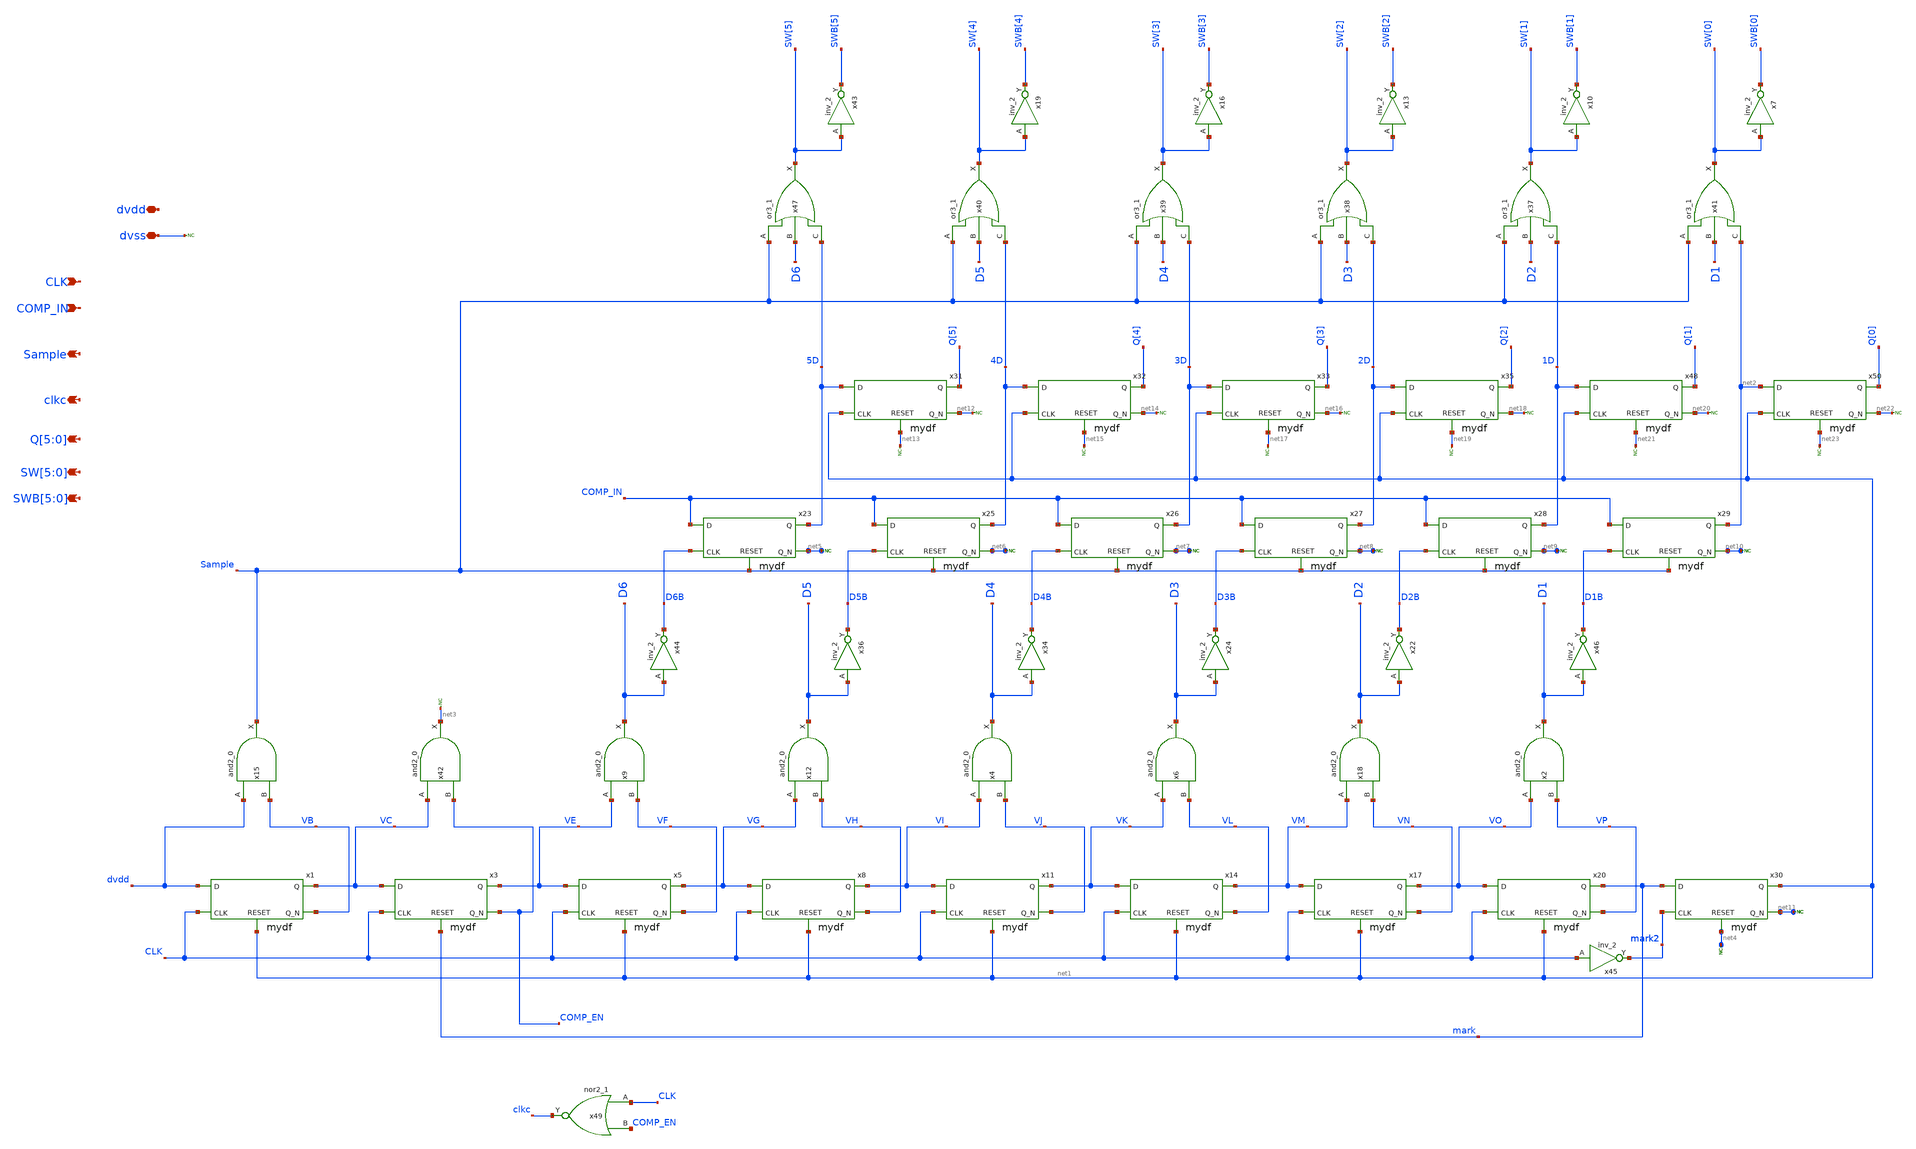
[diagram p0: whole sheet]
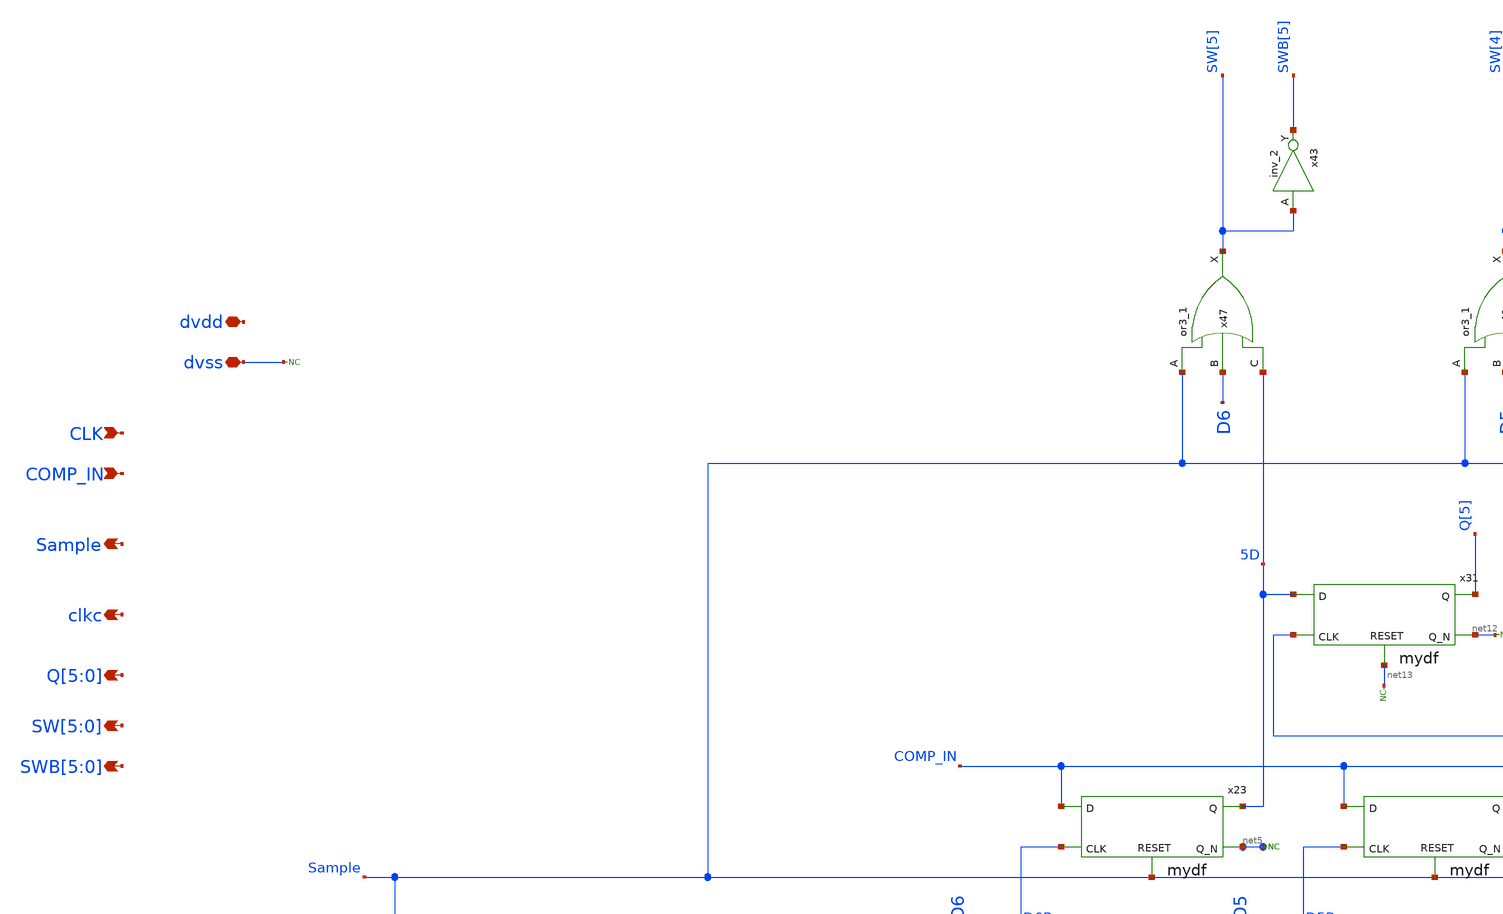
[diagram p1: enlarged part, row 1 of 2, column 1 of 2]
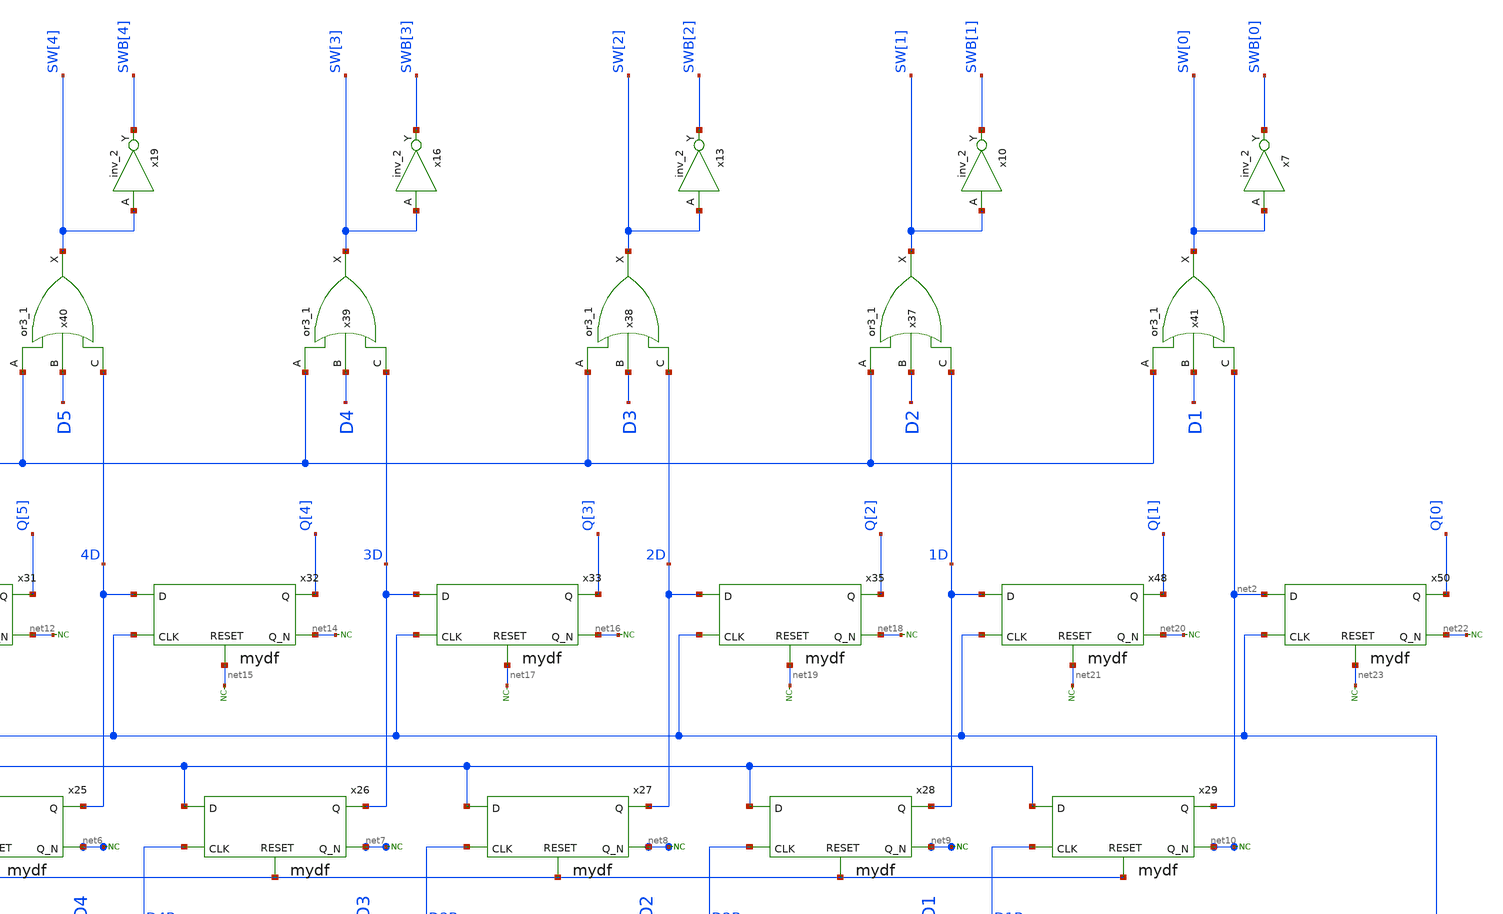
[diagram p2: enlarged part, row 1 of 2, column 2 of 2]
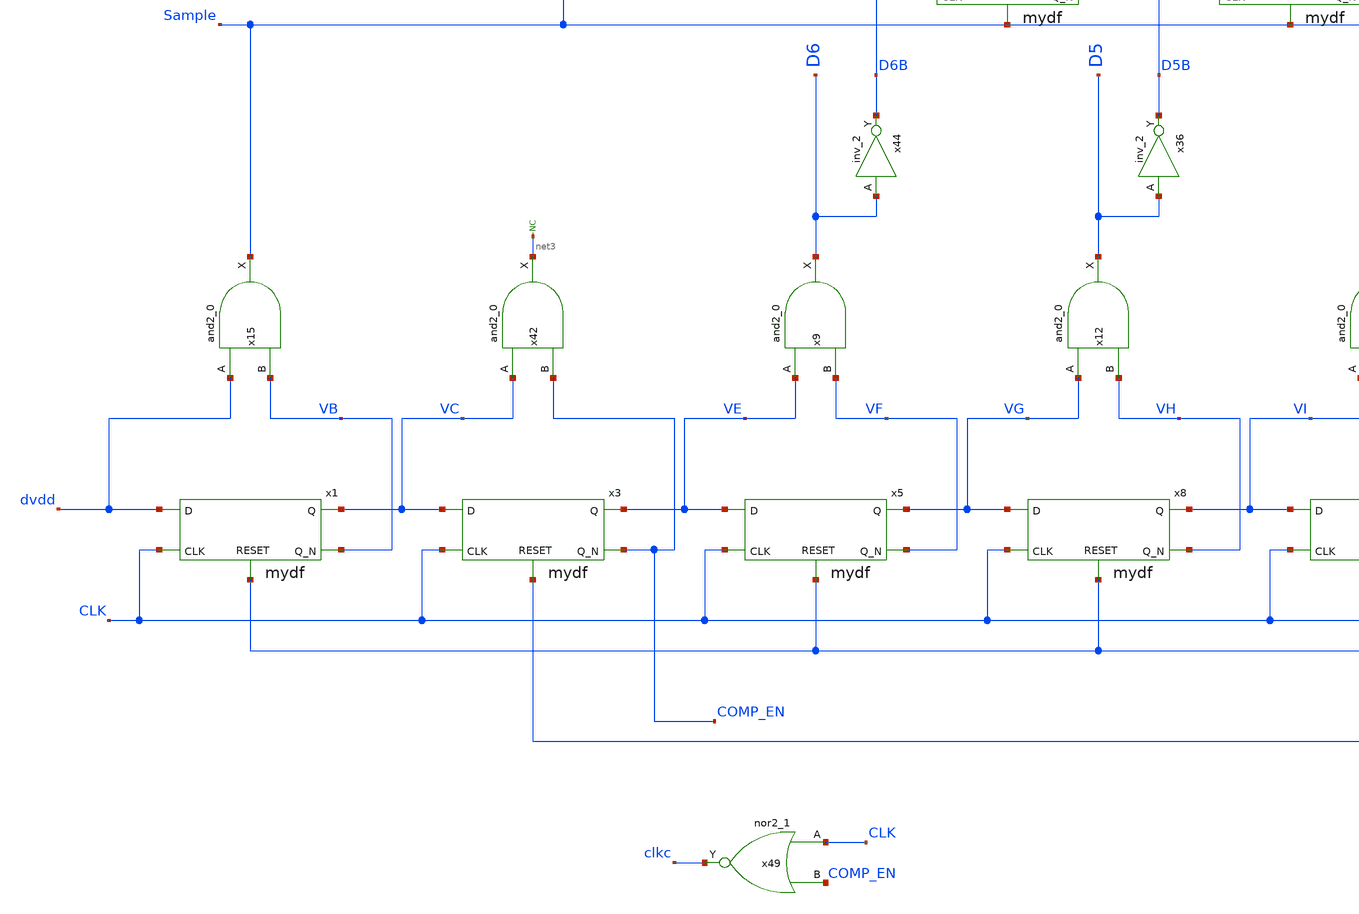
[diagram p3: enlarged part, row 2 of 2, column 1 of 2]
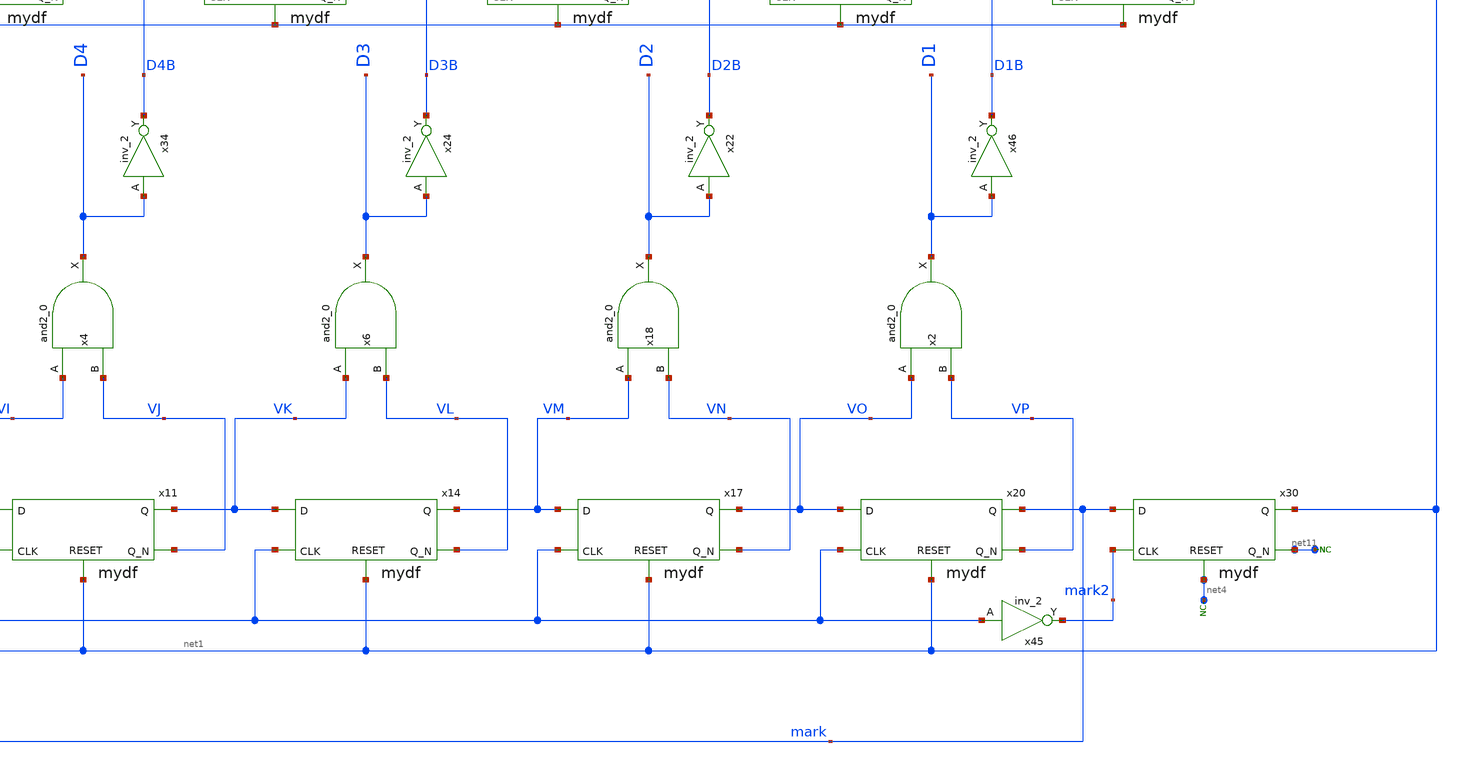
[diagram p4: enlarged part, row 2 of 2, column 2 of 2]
** sch_path: xschem/adc/my_sar_logic.sch
**.subckt my_sar_logic Sample COMP_IN CLK clkc Q[5],Q[4],Q[3],Q[2],Q[1],Q[0]
*+ SW[5],SW[4],SW[3],SW[2],SW[1],SW[0] SWB[5],SWB[4],SWB[3],SWB[2],SWB[1],SWB[0] dvss dvdd
*.opin Sample
*.ipin COMP_IN
*.ipin CLK
*.opin clkc
*.opin Q[5],Q[4],Q[3],Q[2],Q[1],Q[0]
*.opin SW[5],SW[4],SW[3],SW[2],SW[1],SW[0]
*.opin SWB[5],SWB[4],SWB[3],SWB[2],SWB[1],SWB[0]
*.iopin dvss
*.iopin dvdd
x41 Sample D1 net2 avss dvss dvdd dvdd SW[0] sky130_fd_sc_hd__or3_1
x46 D1 dvss dvss dvdd dvdd D1B sky130_fd_sc_hd__inv_2
* noconn #net3
* noconn dvss
x22 D2 dvss dvss dvdd dvdd D2B sky130_fd_sc_hd__inv_2
x24 D3 dvss dvss dvdd dvdd D3B sky130_fd_sc_hd__inv_2
x34 D4 dvss dvss dvdd dvdd D4B sky130_fd_sc_hd__inv_2
x36 D5 dvss dvss dvdd dvdd D5B sky130_fd_sc_hd__inv_2
x44 D6 dvss dvss dvdd dvdd D6B sky130_fd_sc_hd__inv_2
x45 CLK dvss dvss dvdd dvdd mark2 sky130_fd_sc_hd__inv_2
x49 CLK COMP_EN dvss dvss dvdd Vdvdd clkc sky130_fd_sc_hd__nor2_1
x1 CLK VC dvdd VB net1 mydf
x3 CLK VE VC COMP_EN mark mydf
x5 CLK VG VE VF net1 mydf
x8 CLK VI VG VH net1 mydf
x11 CLK VK VI VJ net1 mydf
x14 CLK VM VK VL net1 mydf
x17 CLK VO VM VN net1 mydf
x20 CLK mark VO VP net1 mydf
* noconn #net11
* noconn #net4
* noconn #net11
x23 D6B 5D COMP_IN net5 Sample mydf
* noconn #net5
* noconn #net5
x25 D5B 4D COMP_IN net6 Sample mydf
* noconn #net6
* noconn #net6
x26 D4B 3D COMP_IN net7 Sample mydf
* noconn #net7
* noconn #net7
x27 D3B 2D COMP_IN net8 Sample mydf
* noconn #net8
* noconn #net8
x28 D2B 1D COMP_IN net9 Sample mydf
* noconn #net9
* noconn #net9
x29 D1B net2 COMP_IN net10 Sample mydf
* noconn #net10
* noconn #net10
x30 mark2 net1 mark net11 net4 mydf
* noconn #net11
* noconn #net4
* noconn #net11
x31 net1 Q[5] 5D net12 net13 mydf
* noconn #net12
* noconn #net13
x32 net1 Q[4] 4D net14 net15 mydf
* noconn #net14
* noconn #net15
x33 net1 Q[3] 3D net16 net17 mydf
* noconn #net16
* noconn #net17
x35 net1 Q[2] 2D net18 net19 mydf
* noconn #net18
* noconn #net19
x48 net1 Q[1] 1D net20 net21 mydf
* noconn #net20
* noconn #net21
x50 net1 Q[0] net2 net22 net23 mydf
* noconn #net22
* noconn #net23
x18 VM VN dvss dvss dvdd dvdd D2 sky130_fd_sc_hd__and2_0
x2 VO VP dvss dvss dvdd dvdd D1 sky130_fd_sc_hd__and2_0
x4 VI VJ dvss dvss dvdd dvdd D4 sky130_fd_sc_hd__and2_0
x6 VK VL dvss dvss dvdd dvdd D3 sky130_fd_sc_hd__and2_0
x9 VE VF dvss dvss dvdd dvdd D6 sky130_fd_sc_hd__and2_0
x12 VG VH dvss dvss dvdd dvdd D5 sky130_fd_sc_hd__and2_0
x15 dvdd VB dvss dvss dvdd dvdd Sample sky130_fd_sc_hd__and2_0
x42 VC COMP_EN dvss dvss dvdd dvdd net3 sky130_fd_sc_hd__and2_0
x7 SW[0] dvss dvss dvdd dvdd SWB[0] sky130_fd_sc_hd__inv_2
x10 SW[1] dvss dvss dvdd dvdd SWB[1] sky130_fd_sc_hd__inv_2
x13 SW[2] dvss dvss dvdd dvdd SWB[2] sky130_fd_sc_hd__inv_2
x16 SW[3] dvss dvss dvdd dvdd SWB[3] sky130_fd_sc_hd__inv_2
x19 SW[4] dvss dvss dvdd dvdd SWB[4] sky130_fd_sc_hd__inv_2
x43 SW[5] dvss dvss dvdd dvdd SWB[5] sky130_fd_sc_hd__inv_2
x37 Sample D2 1D avss dvss dvdd dvdd SW[1] sky130_fd_sc_hd__or3_1
x38 Sample D3 2D avss dvss dvdd dvdd SW[2] sky130_fd_sc_hd__or3_1
x39 Sample D4 3D avss dvss dvdd dvdd SW[3] sky130_fd_sc_hd__or3_1
x40 Sample D5 4D avss dvss dvdd dvdd SW[4] sky130_fd_sc_hd__or3_1
x47 Sample D6 5D avss dvss dvdd dvdd SW[5] sky130_fd_sc_hd__or3_1
**.ends

* expanding   symbol:  adc/mydf.sym # of pins=5
** sym_path: xschem/adc/mydf.sym
** sch_path: xschem/adc/mydf.sch
.subckt mydf CLK Q D Q_N RESET
*.ipin CLK
*.ipin D
*.ipin RESET
*.opin Q
*.opin Q_N
x50 CLK D net1 dvss dvss dvdd dvdd Q Q_N sky130_fd_sc_hd__dfrbp_1
x1 RESET dvss dvss dvdd dvdd net1 sky130_fd_sc_hd__inv_1
.ends

.end
